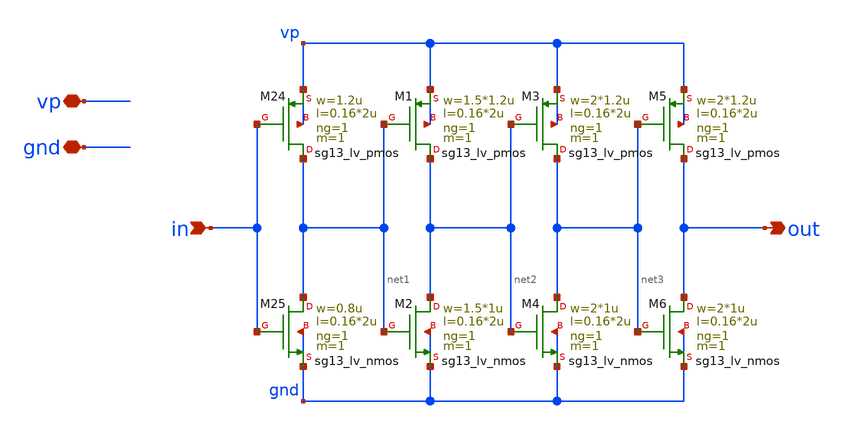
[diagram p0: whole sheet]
** sch_path: schematics/vco/vco_cell/0_buf.sch
**.subckt 0_buf in out vp gnd
*.ipin in
*.opin out
*.iopin vp
*.iopin gnd
XM24 net1 in vp vp sg13_lv_pmos w=1.2u l=0.16*2u ng=1 m=1 mm_ok=1
XM25 net1 in gnd gnd sg13_lv_nmos w=0.8u l=0.16*2u ng=1 m=1 mm_ok=1
XM1 net2 net1 vp vp sg13_lv_pmos w=1.5*1.2u l=0.16*2u ng=1 m=1 mm_ok=1
XM2 net2 net1 gnd gnd sg13_lv_nmos w=1.5*1u l=0.16*2u ng=1 m=1 mm_ok=1
XM3 net3 net2 vp vp sg13_lv_pmos w=2*1.2u l=0.16*2u ng=1 m=1 mm_ok=1
XM4 net3 net2 gnd gnd sg13_lv_nmos w=2*1u l=0.16*2u ng=1 m=1 mm_ok=1
XM5 out net3 vp vp sg13_lv_pmos w=2*1.2u l=0.16*2u ng=1 m=1 mm_ok=1
XM6 out net3 gnd gnd sg13_lv_nmos w=2*1u l=0.16*2u ng=1 m=1 mm_ok=1
**.ends
.end
